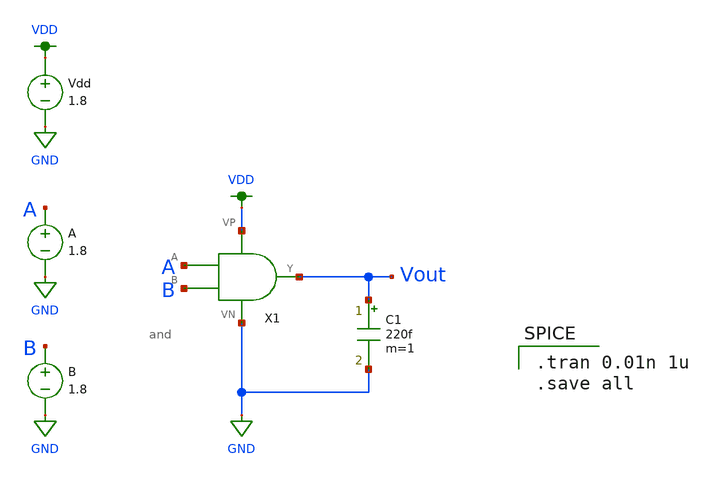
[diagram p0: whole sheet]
** sch_path: MP1/and_tran.sch
**.subckt and_tran
C1 Vout GND 220f m=1
Vdd VDD GND 1.8
X1 A B Vout VDD GND and
A A GND 1.8
B B GND 1.8
**** begin user architecture code

.option wnflag=1
.lib ~/skywater/skywater-pdk/libraries/sky130_fd_pr_ngspice/latest/models/sky130.lib.spice tt


.tran 0.01n 1u
.save all

**** end user architecture code
**.ends
.GLOBAL VDD
.GLOBAL GND
.end
